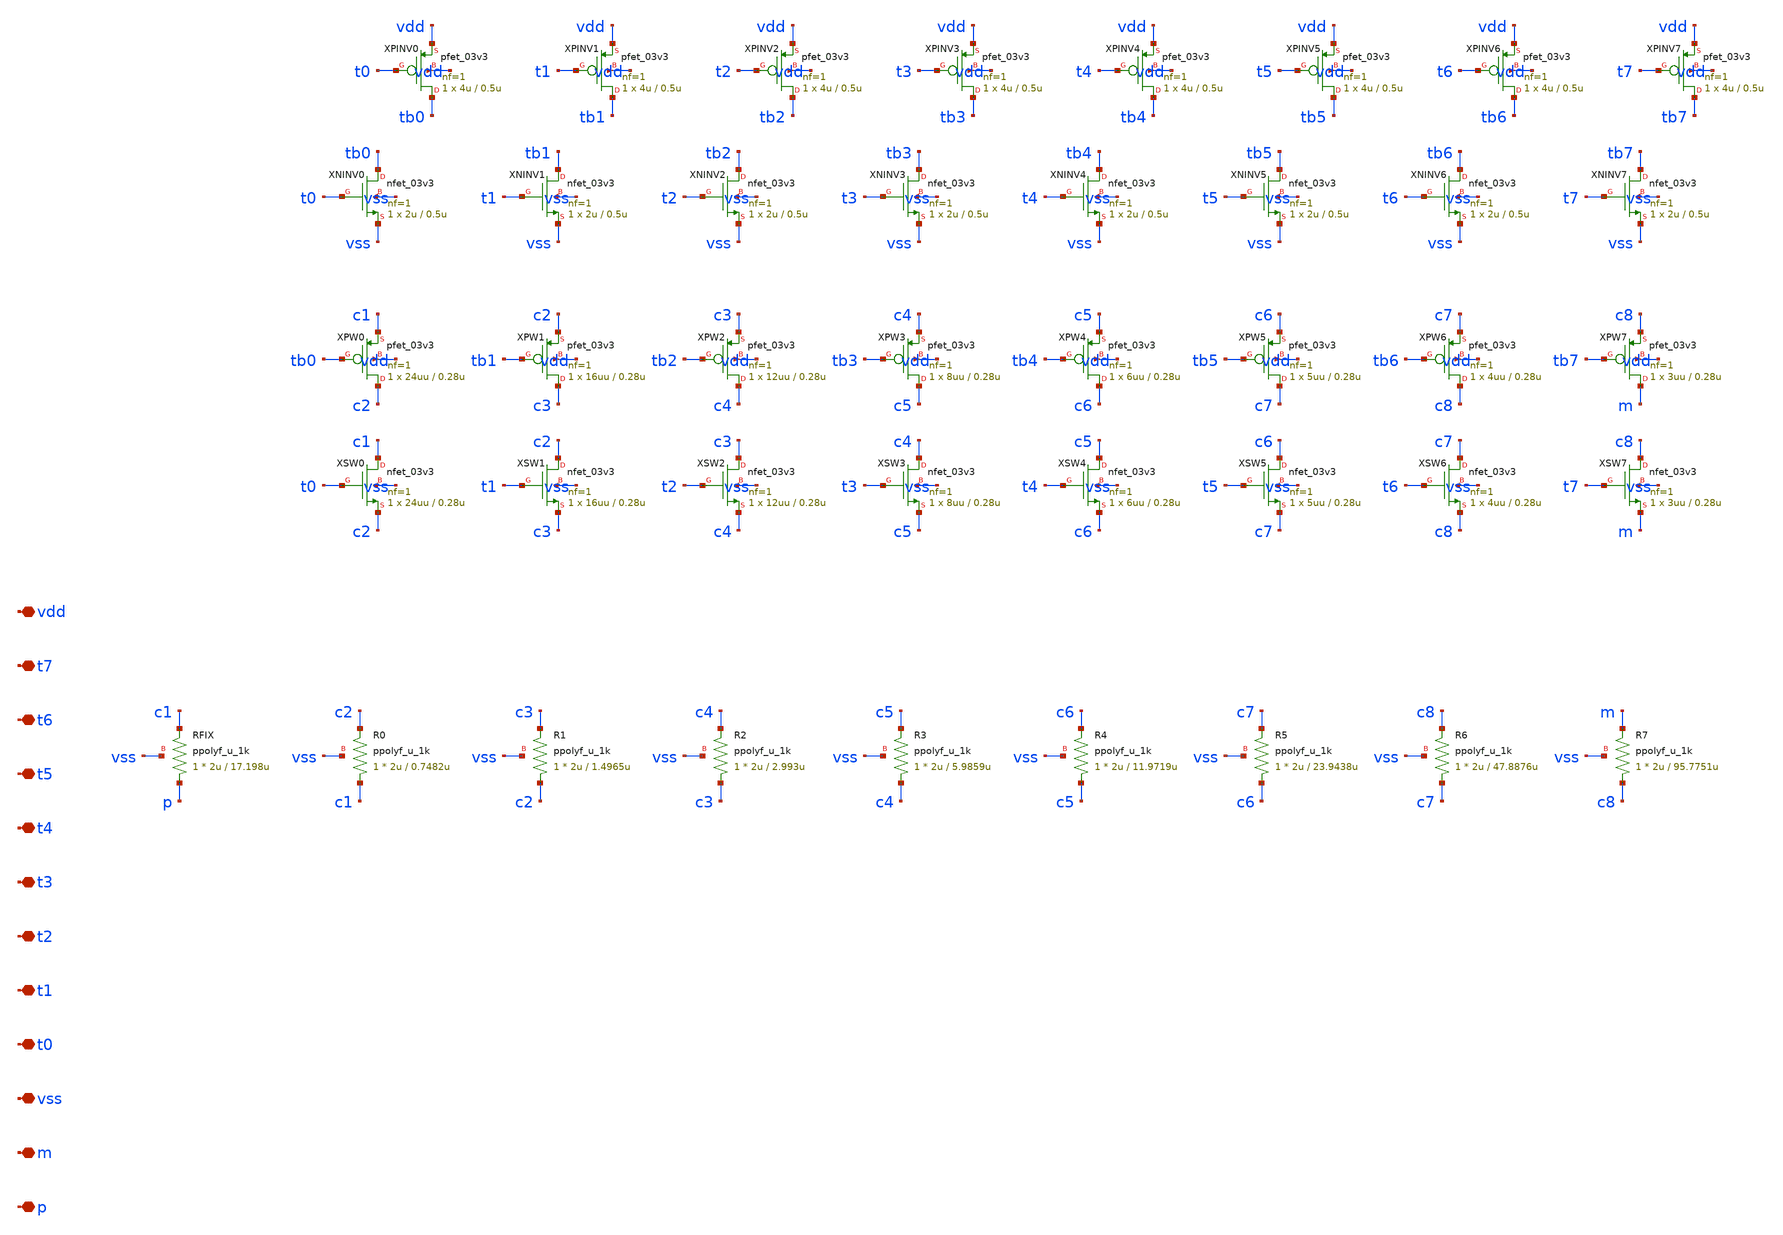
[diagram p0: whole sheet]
** sch_path: design/rcosc_trim_bank.sch
**.subckt rcosc_trim_bank p m vss t0 t1 t2 t3 t4 t5 t6 t7 vdd
*.iopin p
*.iopin m
*.iopin vss
*.iopin t0
*.iopin t1
*.iopin t2
*.iopin t3
*.iopin t4
*.iopin t5
*.iopin t6
*.iopin t7
*.iopin vdd
XRFIX p c1 vss ppolyf_u_1k r_width=2u r_length=17.198u m=1
XR0 c1 c2 vss ppolyf_u_1k r_width=2u r_length=0.7482u m=1
XSW0 c1 t0 c2 vss nfet_03v3 L=0.28u W=24uu nf=1 ad='int((nf+1)/2) * W/nf * 0.18u' as='int((nf+2)/2) * W/nf * 0.18u'
+ pd='2*int((nf+1)/2) * (W/nf + 0.18u)' ps='2*int((nf+2)/2) * (W/nf + 0.18u)' nrd='0.18u / W' nrs='0.18u / W'
+ sa=0 sb=0 sd=0 m=1
XPW0 c2 tb0 c1 vdd pfet_03v3 L=0.28u W=24uu nf=1 ad='int((nf+1)/2) * W/nf * 0.18u' as='int((nf+2)/2) * W/nf * 0.18u'
+ pd='2*int((nf+1)/2) * (W/nf + 0.18u)' ps='2*int((nf+2)/2) * (W/nf + 0.18u)' nrd='0.18u / W' nrs='0.18u / W'
+ sa=0 sb=0 sd=0 m=1
XNINV0 tb0 t0 vss vss nfet_03v3 L=0.5u W=2u nf=1 ad='int((nf+1)/2) * W/nf * 0.18u' as='int((nf+2)/2) * W/nf * 0.18u'
+ pd='2*int((nf+1)/2) * (W/nf + 0.18u)' ps='2*int((nf+2)/2) * (W/nf + 0.18u)' nrd='0.18u / W' nrs='0.18u / W'
+ sa=0 sb=0 sd=0 m=1
XPINV0 tb0 t0 vdd vdd pfet_03v3 L=0.5u W=4u nf=1 ad='int((nf+1)/2) * W/nf * 0.18u' as='int((nf+2)/2) * W/nf * 0.18u'
+ pd='2*int((nf+1)/2) * (W/nf + 0.18u)' ps='2*int((nf+2)/2) * (W/nf + 0.18u)' nrd='0.18u / W' nrs='0.18u / W'
+ sa=0 sb=0 sd=0 m=1
XR1 c2 c3 vss ppolyf_u_1k r_width=2u r_length=1.4965u m=1
XSW1 c2 t1 c3 vss nfet_03v3 L=0.28u W=16uu nf=1 ad='int((nf+1)/2) * W/nf * 0.18u' as='int((nf+2)/2) * W/nf * 0.18u'
+ pd='2*int((nf+1)/2) * (W/nf + 0.18u)' ps='2*int((nf+2)/2) * (W/nf + 0.18u)' nrd='0.18u / W' nrs='0.18u / W'
+ sa=0 sb=0 sd=0 m=1
XPW1 c3 tb1 c2 vdd pfet_03v3 L=0.28u W=16uu nf=1 ad='int((nf+1)/2) * W/nf * 0.18u' as='int((nf+2)/2) * W/nf * 0.18u'
+ pd='2*int((nf+1)/2) * (W/nf + 0.18u)' ps='2*int((nf+2)/2) * (W/nf + 0.18u)' nrd='0.18u / W' nrs='0.18u / W'
+ sa=0 sb=0 sd=0 m=1
XNINV1 tb1 t1 vss vss nfet_03v3 L=0.5u W=2u nf=1 ad='int((nf+1)/2) * W/nf * 0.18u' as='int((nf+2)/2) * W/nf * 0.18u'
+ pd='2*int((nf+1)/2) * (W/nf + 0.18u)' ps='2*int((nf+2)/2) * (W/nf + 0.18u)' nrd='0.18u / W' nrs='0.18u / W'
+ sa=0 sb=0 sd=0 m=1
XPINV1 tb1 t1 vdd vdd pfet_03v3 L=0.5u W=4u nf=1 ad='int((nf+1)/2) * W/nf * 0.18u' as='int((nf+2)/2) * W/nf * 0.18u'
+ pd='2*int((nf+1)/2) * (W/nf + 0.18u)' ps='2*int((nf+2)/2) * (W/nf + 0.18u)' nrd='0.18u / W' nrs='0.18u / W'
+ sa=0 sb=0 sd=0 m=1
XR2 c3 c4 vss ppolyf_u_1k r_width=2u r_length=2.993u m=1
XSW2 c3 t2 c4 vss nfet_03v3 L=0.28u W=12uu nf=1 ad='int((nf+1)/2) * W/nf * 0.18u' as='int((nf+2)/2) * W/nf * 0.18u'
+ pd='2*int((nf+1)/2) * (W/nf + 0.18u)' ps='2*int((nf+2)/2) * (W/nf + 0.18u)' nrd='0.18u / W' nrs='0.18u / W'
+ sa=0 sb=0 sd=0 m=1
XPW2 c4 tb2 c3 vdd pfet_03v3 L=0.28u W=12uu nf=1 ad='int((nf+1)/2) * W/nf * 0.18u' as='int((nf+2)/2) * W/nf * 0.18u'
+ pd='2*int((nf+1)/2) * (W/nf + 0.18u)' ps='2*int((nf+2)/2) * (W/nf + 0.18u)' nrd='0.18u / W' nrs='0.18u / W'
+ sa=0 sb=0 sd=0 m=1
XNINV2 tb2 t2 vss vss nfet_03v3 L=0.5u W=2u nf=1 ad='int((nf+1)/2) * W/nf * 0.18u' as='int((nf+2)/2) * W/nf * 0.18u'
+ pd='2*int((nf+1)/2) * (W/nf + 0.18u)' ps='2*int((nf+2)/2) * (W/nf + 0.18u)' nrd='0.18u / W' nrs='0.18u / W'
+ sa=0 sb=0 sd=0 m=1
XPINV2 tb2 t2 vdd vdd pfet_03v3 L=0.5u W=4u nf=1 ad='int((nf+1)/2) * W/nf * 0.18u' as='int((nf+2)/2) * W/nf * 0.18u'
+ pd='2*int((nf+1)/2) * (W/nf + 0.18u)' ps='2*int((nf+2)/2) * (W/nf + 0.18u)' nrd='0.18u / W' nrs='0.18u / W'
+ sa=0 sb=0 sd=0 m=1
XR3 c4 c5 vss ppolyf_u_1k r_width=2u r_length=5.9859u m=1
XSW3 c4 t3 c5 vss nfet_03v3 L=0.28u W=8uu nf=1 ad='int((nf+1)/2) * W/nf * 0.18u' as='int((nf+2)/2) * W/nf * 0.18u'
+ pd='2*int((nf+1)/2) * (W/nf + 0.18u)' ps='2*int((nf+2)/2) * (W/nf + 0.18u)' nrd='0.18u / W' nrs='0.18u / W'
+ sa=0 sb=0 sd=0 m=1
XPW3 c5 tb3 c4 vdd pfet_03v3 L=0.28u W=8uu nf=1 ad='int((nf+1)/2) * W/nf * 0.18u' as='int((nf+2)/2) * W/nf * 0.18u'
+ pd='2*int((nf+1)/2) * (W/nf + 0.18u)' ps='2*int((nf+2)/2) * (W/nf + 0.18u)' nrd='0.18u / W' nrs='0.18u / W'
+ sa=0 sb=0 sd=0 m=1
XNINV3 tb3 t3 vss vss nfet_03v3 L=0.5u W=2u nf=1 ad='int((nf+1)/2) * W/nf * 0.18u' as='int((nf+2)/2) * W/nf * 0.18u'
+ pd='2*int((nf+1)/2) * (W/nf + 0.18u)' ps='2*int((nf+2)/2) * (W/nf + 0.18u)' nrd='0.18u / W' nrs='0.18u / W'
+ sa=0 sb=0 sd=0 m=1
XPINV3 tb3 t3 vdd vdd pfet_03v3 L=0.5u W=4u nf=1 ad='int((nf+1)/2) * W/nf * 0.18u' as='int((nf+2)/2) * W/nf * 0.18u'
+ pd='2*int((nf+1)/2) * (W/nf + 0.18u)' ps='2*int((nf+2)/2) * (W/nf + 0.18u)' nrd='0.18u / W' nrs='0.18u / W'
+ sa=0 sb=0 sd=0 m=1
XR4 c5 c6 vss ppolyf_u_1k r_width=2u r_length=11.9719u m=1
XSW4 c5 t4 c6 vss nfet_03v3 L=0.28u W=6uu nf=1 ad='int((nf+1)/2) * W/nf * 0.18u' as='int((nf+2)/2) * W/nf * 0.18u'
+ pd='2*int((nf+1)/2) * (W/nf + 0.18u)' ps='2*int((nf+2)/2) * (W/nf + 0.18u)' nrd='0.18u / W' nrs='0.18u / W'
+ sa=0 sb=0 sd=0 m=1
XPW4 c6 tb4 c5 vdd pfet_03v3 L=0.28u W=6uu nf=1 ad='int((nf+1)/2) * W/nf * 0.18u' as='int((nf+2)/2) * W/nf * 0.18u'
+ pd='2*int((nf+1)/2) * (W/nf + 0.18u)' ps='2*int((nf+2)/2) * (W/nf + 0.18u)' nrd='0.18u / W' nrs='0.18u / W'
+ sa=0 sb=0 sd=0 m=1
XNINV4 tb4 t4 vss vss nfet_03v3 L=0.5u W=2u nf=1 ad='int((nf+1)/2) * W/nf * 0.18u' as='int((nf+2)/2) * W/nf * 0.18u'
+ pd='2*int((nf+1)/2) * (W/nf + 0.18u)' ps='2*int((nf+2)/2) * (W/nf + 0.18u)' nrd='0.18u / W' nrs='0.18u / W'
+ sa=0 sb=0 sd=0 m=1
XPINV4 tb4 t4 vdd vdd pfet_03v3 L=0.5u W=4u nf=1 ad='int((nf+1)/2) * W/nf * 0.18u' as='int((nf+2)/2) * W/nf * 0.18u'
+ pd='2*int((nf+1)/2) * (W/nf + 0.18u)' ps='2*int((nf+2)/2) * (W/nf + 0.18u)' nrd='0.18u / W' nrs='0.18u / W'
+ sa=0 sb=0 sd=0 m=1
XR5 c6 c7 vss ppolyf_u_1k r_width=2u r_length=23.9438u m=1
XSW5 c6 t5 c7 vss nfet_03v3 L=0.28u W=5uu nf=1 ad='int((nf+1)/2) * W/nf * 0.18u' as='int((nf+2)/2) * W/nf * 0.18u'
+ pd='2*int((nf+1)/2) * (W/nf + 0.18u)' ps='2*int((nf+2)/2) * (W/nf + 0.18u)' nrd='0.18u / W' nrs='0.18u / W'
+ sa=0 sb=0 sd=0 m=1
XPW5 c7 tb5 c6 vdd pfet_03v3 L=0.28u W=5uu nf=1 ad='int((nf+1)/2) * W/nf * 0.18u' as='int((nf+2)/2) * W/nf * 0.18u'
+ pd='2*int((nf+1)/2) * (W/nf + 0.18u)' ps='2*int((nf+2)/2) * (W/nf + 0.18u)' nrd='0.18u / W' nrs='0.18u / W'
+ sa=0 sb=0 sd=0 m=1
XNINV5 tb5 t5 vss vss nfet_03v3 L=0.5u W=2u nf=1 ad='int((nf+1)/2) * W/nf * 0.18u' as='int((nf+2)/2) * W/nf * 0.18u'
+ pd='2*int((nf+1)/2) * (W/nf + 0.18u)' ps='2*int((nf+2)/2) * (W/nf + 0.18u)' nrd='0.18u / W' nrs='0.18u / W'
+ sa=0 sb=0 sd=0 m=1
XPINV5 tb5 t5 vdd vdd pfet_03v3 L=0.5u W=4u nf=1 ad='int((nf+1)/2) * W/nf * 0.18u' as='int((nf+2)/2) * W/nf * 0.18u'
+ pd='2*int((nf+1)/2) * (W/nf + 0.18u)' ps='2*int((nf+2)/2) * (W/nf + 0.18u)' nrd='0.18u / W' nrs='0.18u / W'
+ sa=0 sb=0 sd=0 m=1
XR6 c7 c8 vss ppolyf_u_1k r_width=2u r_length=47.8876u m=1
XSW6 c7 t6 c8 vss nfet_03v3 L=0.28u W=4uu nf=1 ad='int((nf+1)/2) * W/nf * 0.18u' as='int((nf+2)/2) * W/nf * 0.18u'
+ pd='2*int((nf+1)/2) * (W/nf + 0.18u)' ps='2*int((nf+2)/2) * (W/nf + 0.18u)' nrd='0.18u / W' nrs='0.18u / W'
+ sa=0 sb=0 sd=0 m=1
XPW6 c8 tb6 c7 vdd pfet_03v3 L=0.28u W=4uu nf=1 ad='int((nf+1)/2) * W/nf * 0.18u' as='int((nf+2)/2) * W/nf * 0.18u'
+ pd='2*int((nf+1)/2) * (W/nf + 0.18u)' ps='2*int((nf+2)/2) * (W/nf + 0.18u)' nrd='0.18u / W' nrs='0.18u / W'
+ sa=0 sb=0 sd=0 m=1
XNINV6 tb6 t6 vss vss nfet_03v3 L=0.5u W=2u nf=1 ad='int((nf+1)/2) * W/nf * 0.18u' as='int((nf+2)/2) * W/nf * 0.18u'
+ pd='2*int((nf+1)/2) * (W/nf + 0.18u)' ps='2*int((nf+2)/2) * (W/nf + 0.18u)' nrd='0.18u / W' nrs='0.18u / W'
+ sa=0 sb=0 sd=0 m=1
XPINV6 tb6 t6 vdd vdd pfet_03v3 L=0.5u W=4u nf=1 ad='int((nf+1)/2) * W/nf * 0.18u' as='int((nf+2)/2) * W/nf * 0.18u'
+ pd='2*int((nf+1)/2) * (W/nf + 0.18u)' ps='2*int((nf+2)/2) * (W/nf + 0.18u)' nrd='0.18u / W' nrs='0.18u / W'
+ sa=0 sb=0 sd=0 m=1
XR7 c8 m vss ppolyf_u_1k r_width=2u r_length=95.7751u m=1
XSW7 c8 t7 m vss nfet_03v3 L=0.28u W=3uu nf=1 ad='int((nf+1)/2) * W/nf * 0.18u' as='int((nf+2)/2) * W/nf * 0.18u'
+ pd='2*int((nf+1)/2) * (W/nf + 0.18u)' ps='2*int((nf+2)/2) * (W/nf + 0.18u)' nrd='0.18u / W' nrs='0.18u / W'
+ sa=0 sb=0 sd=0 m=1
XPW7 m tb7 c8 vdd pfet_03v3 L=0.28u W=3uu nf=1 ad='int((nf+1)/2) * W/nf * 0.18u' as='int((nf+2)/2) * W/nf * 0.18u'
+ pd='2*int((nf+1)/2) * (W/nf + 0.18u)' ps='2*int((nf+2)/2) * (W/nf + 0.18u)' nrd='0.18u / W' nrs='0.18u / W'
+ sa=0 sb=0 sd=0 m=1
XNINV7 tb7 t7 vss vss nfet_03v3 L=0.5u W=2u nf=1 ad='int((nf+1)/2) * W/nf * 0.18u' as='int((nf+2)/2) * W/nf * 0.18u'
+ pd='2*int((nf+1)/2) * (W/nf + 0.18u)' ps='2*int((nf+2)/2) * (W/nf + 0.18u)' nrd='0.18u / W' nrs='0.18u / W'
+ sa=0 sb=0 sd=0 m=1
XPINV7 tb7 t7 vdd vdd pfet_03v3 L=0.5u W=4u nf=1 ad='int((nf+1)/2) * W/nf * 0.18u' as='int((nf+2)/2) * W/nf * 0.18u'
+ pd='2*int((nf+1)/2) * (W/nf + 0.18u)' ps='2*int((nf+2)/2) * (W/nf + 0.18u)' nrd='0.18u / W' nrs='0.18u / W'
+ sa=0 sb=0 sd=0 m=1
**.ends
.end
